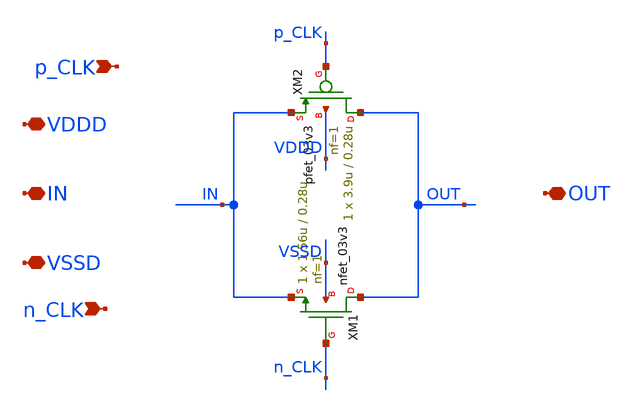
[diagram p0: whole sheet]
** sch_path: SAR_ADC/SAR_Asynchronous_Logic/xschem/SAR_Asynchronous_Logic_tgate.sch
**.subckt SAR_Asynchronous_Logic_tgate IN VDDD VSSD n_CLK p_CLK OUT
*.iopin IN
*.iopin VDDD
*.iopin VSSD
*.ipin n_CLK
*.ipin p_CLK
*.iopin OUT
XM1 OUT n_CLK IN VSSD nfet_03v3 L=0.28u W=1.56u nf=1 ad='int((nf+1)/2) * W/nf * 0.18u' as='int((nf+2)/2) * W/nf * 0.18u'
+ pd='2*int((nf+1)/2) * (W/nf + 0.18u)' ps='2*int((nf+2)/2) * (W/nf + 0.18u)' nrd='0.18u / W' nrs='0.18u / W'
+ sa=0 sb=0 sd=0 m=1
XM2 OUT p_CLK IN VDDD pfet_03v3 L=0.28u W=3.9u nf=1 ad='int((nf+1)/2) * W/nf * 0.18u' as='int((nf+2)/2) * W/nf * 0.18u'
+ pd='2*int((nf+1)/2) * (W/nf + 0.18u)' ps='2*int((nf+2)/2) * (W/nf + 0.18u)' nrd='0.18u / W' nrs='0.18u / W'
+ sa=0 sb=0 sd=0 m=1
**.ends
.end
